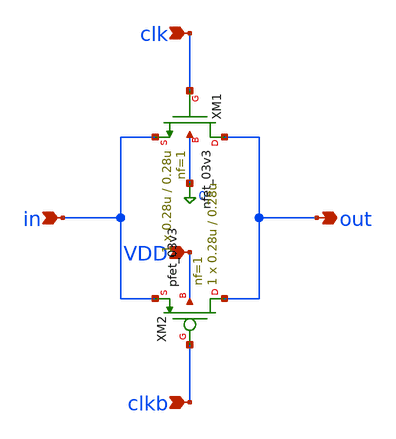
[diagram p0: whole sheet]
** sch_path: Design_Files/IC Design/Schematic/SAR_ADC_BLOCKS/TG_SW/TG_SW.sch
**.subckt TG_SW in clk clkb out VDD
*.ipin in
*.ipin clk
*.ipin clkb
*.opin out
*.ipin VDD
XM1 out clk in 0 nfet_03v3 L=0.28u W=0.28u nf=1 ad='int((nf+1)/2) * W/nf * 0.18u' as='int((nf+2)/2) * W/nf * 0.18u'
+ pd='2*int((nf+1)/2) * (W/nf + 0.18u)' ps='2*int((nf+2)/2) * (W/nf + 0.18u)' nrd='0.18u / W' nrs='0.18u / W'
+ sa=0 sb=0 sd=0 m=1
XM2 out clkb in VDD pfet_03v3 L=0.28u W=0.28u nf=1 ad='int((nf+1)/2) * W/nf * 0.18u' as='int((nf+2)/2) * W/nf * 0.18u'
+ pd='2*int((nf+1)/2) * (W/nf + 0.18u)' ps='2*int((nf+2)/2) * (W/nf + 0.18u)' nrd='0.18u / W' nrs='0.18u / W'
+ sa=0 sb=0 sd=0 m=1
**.ends
.end
